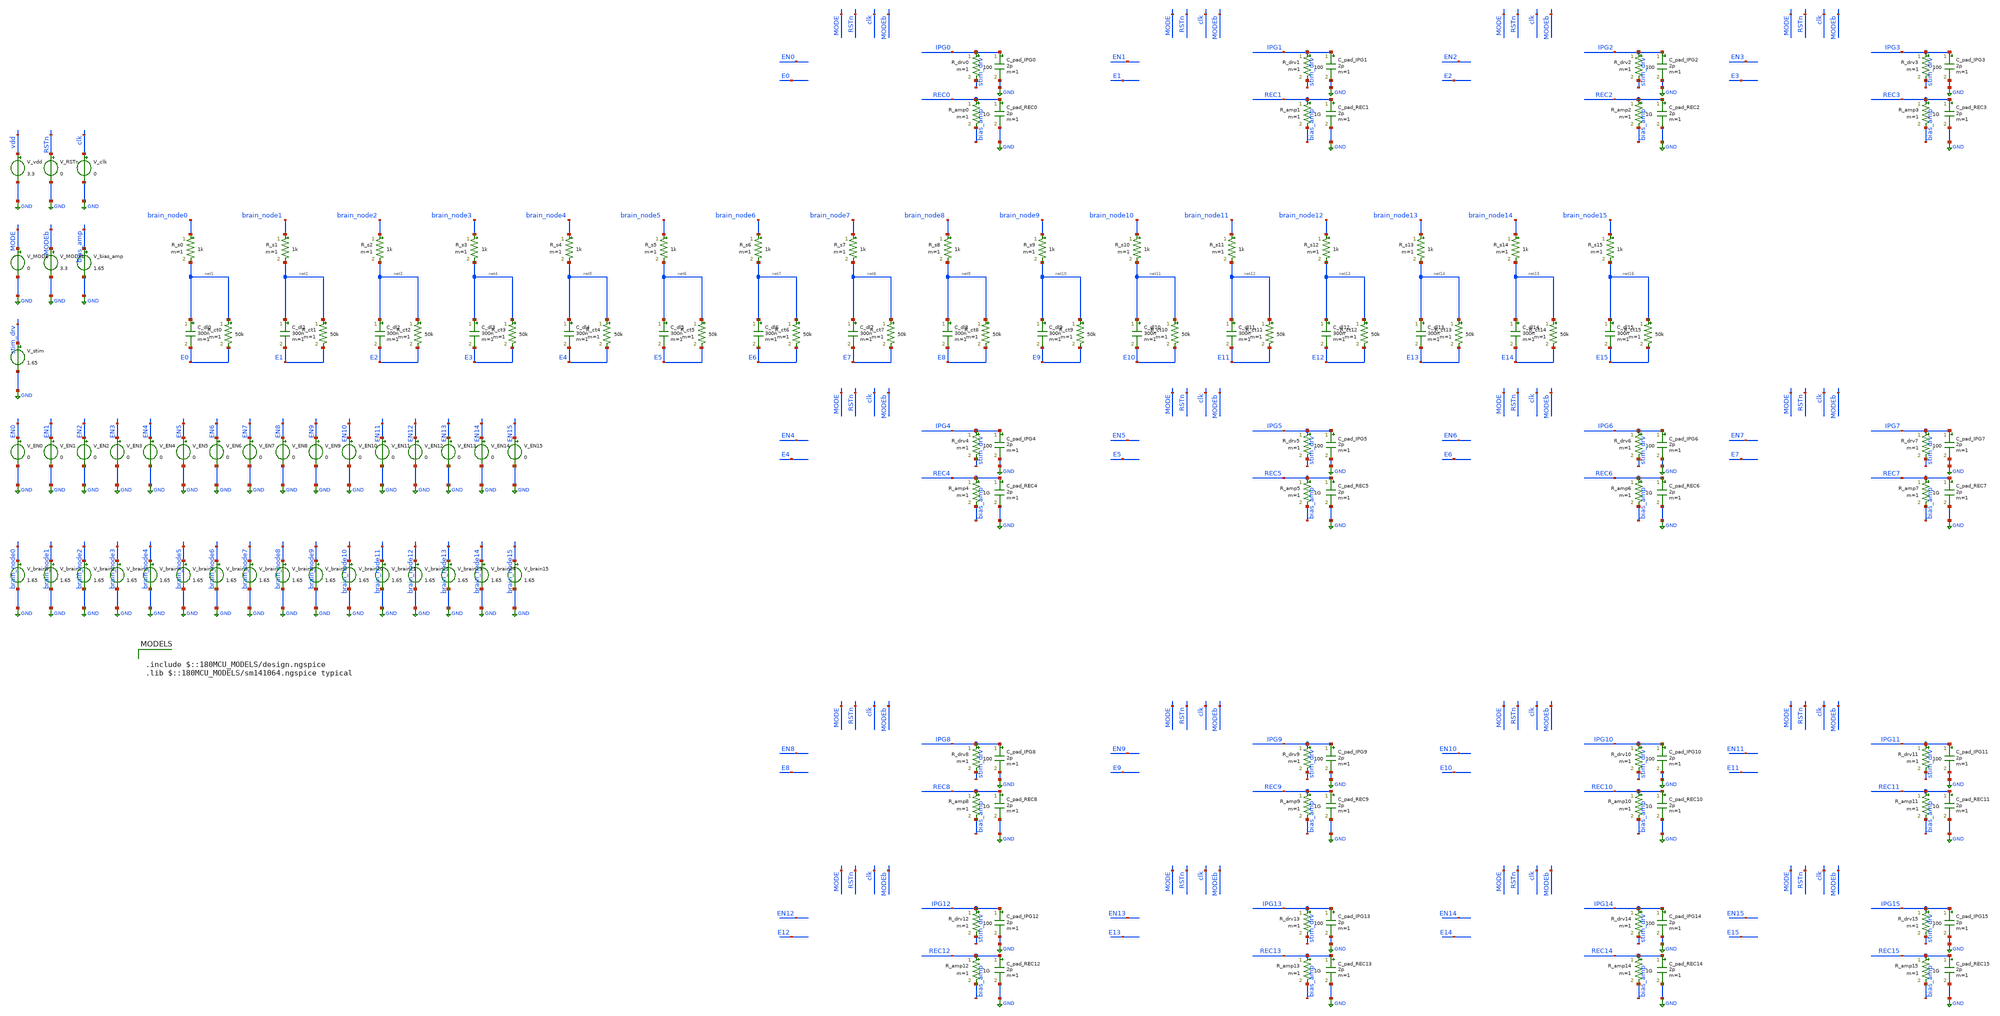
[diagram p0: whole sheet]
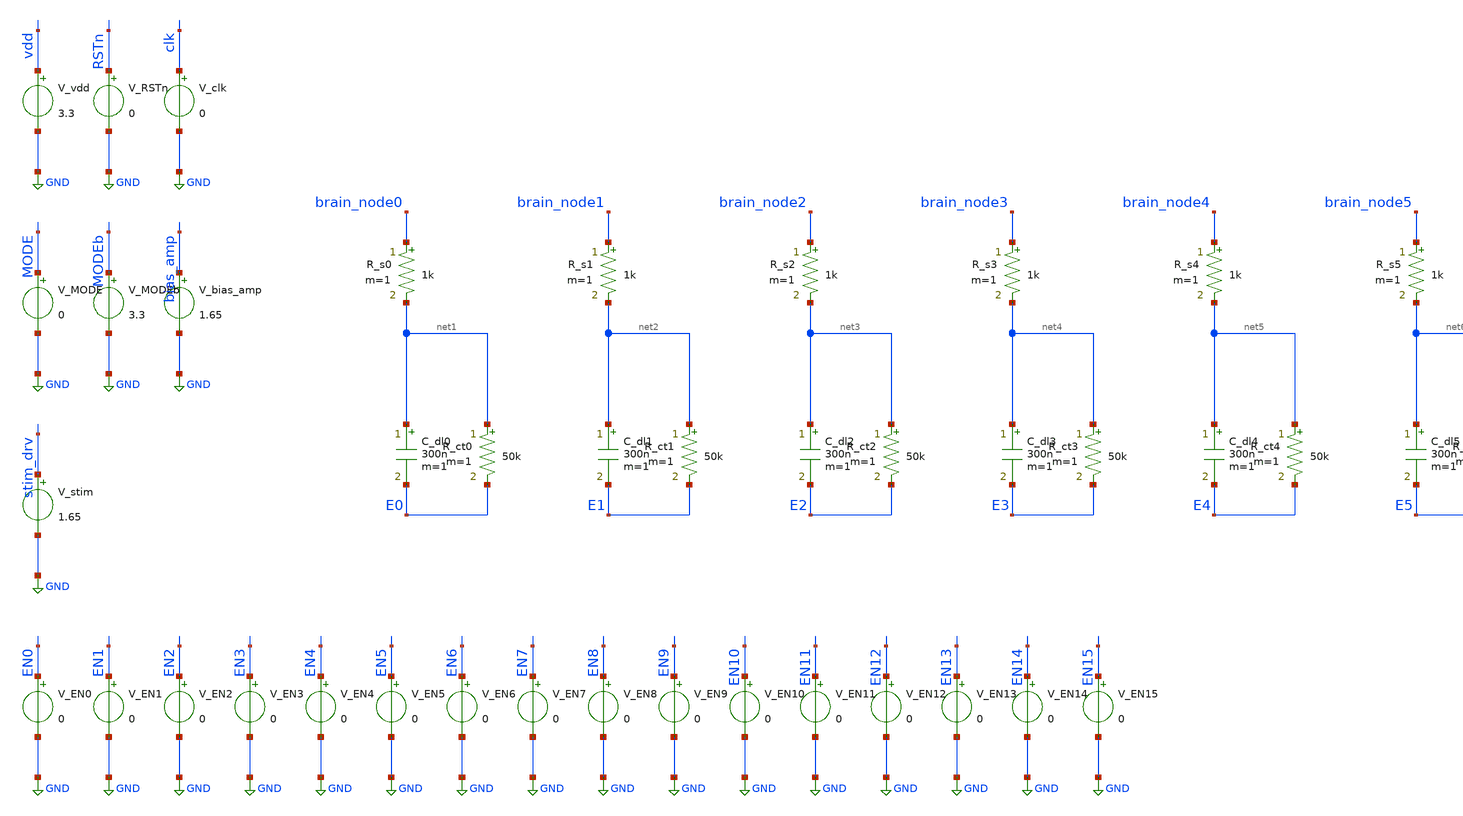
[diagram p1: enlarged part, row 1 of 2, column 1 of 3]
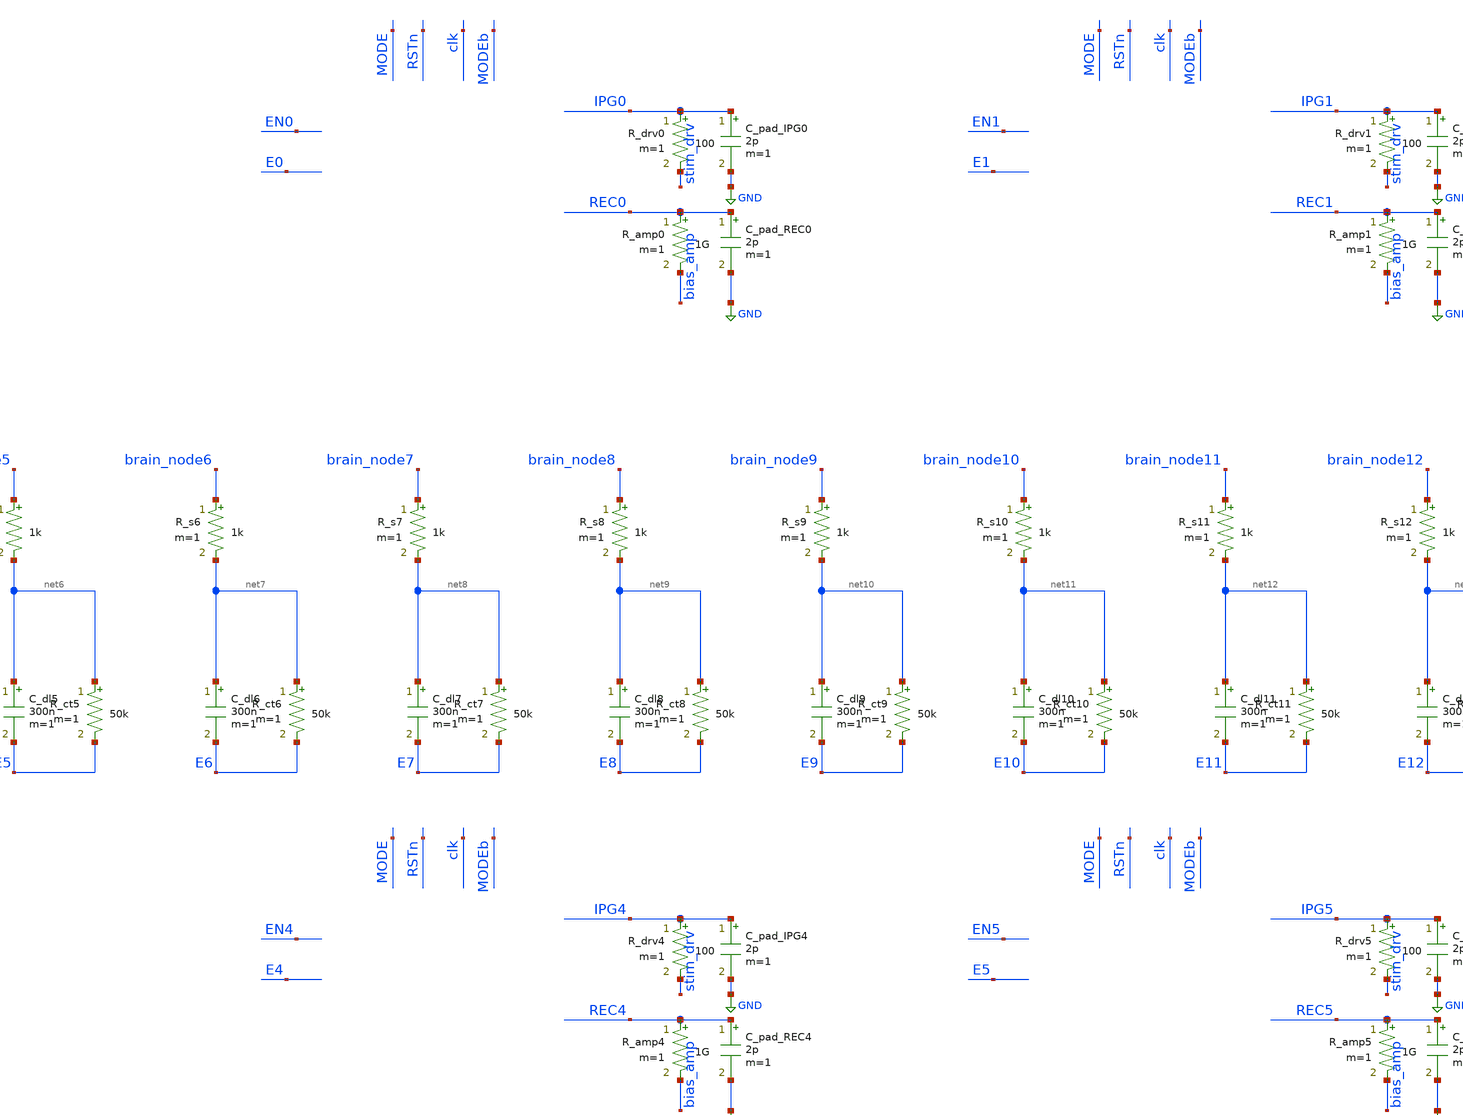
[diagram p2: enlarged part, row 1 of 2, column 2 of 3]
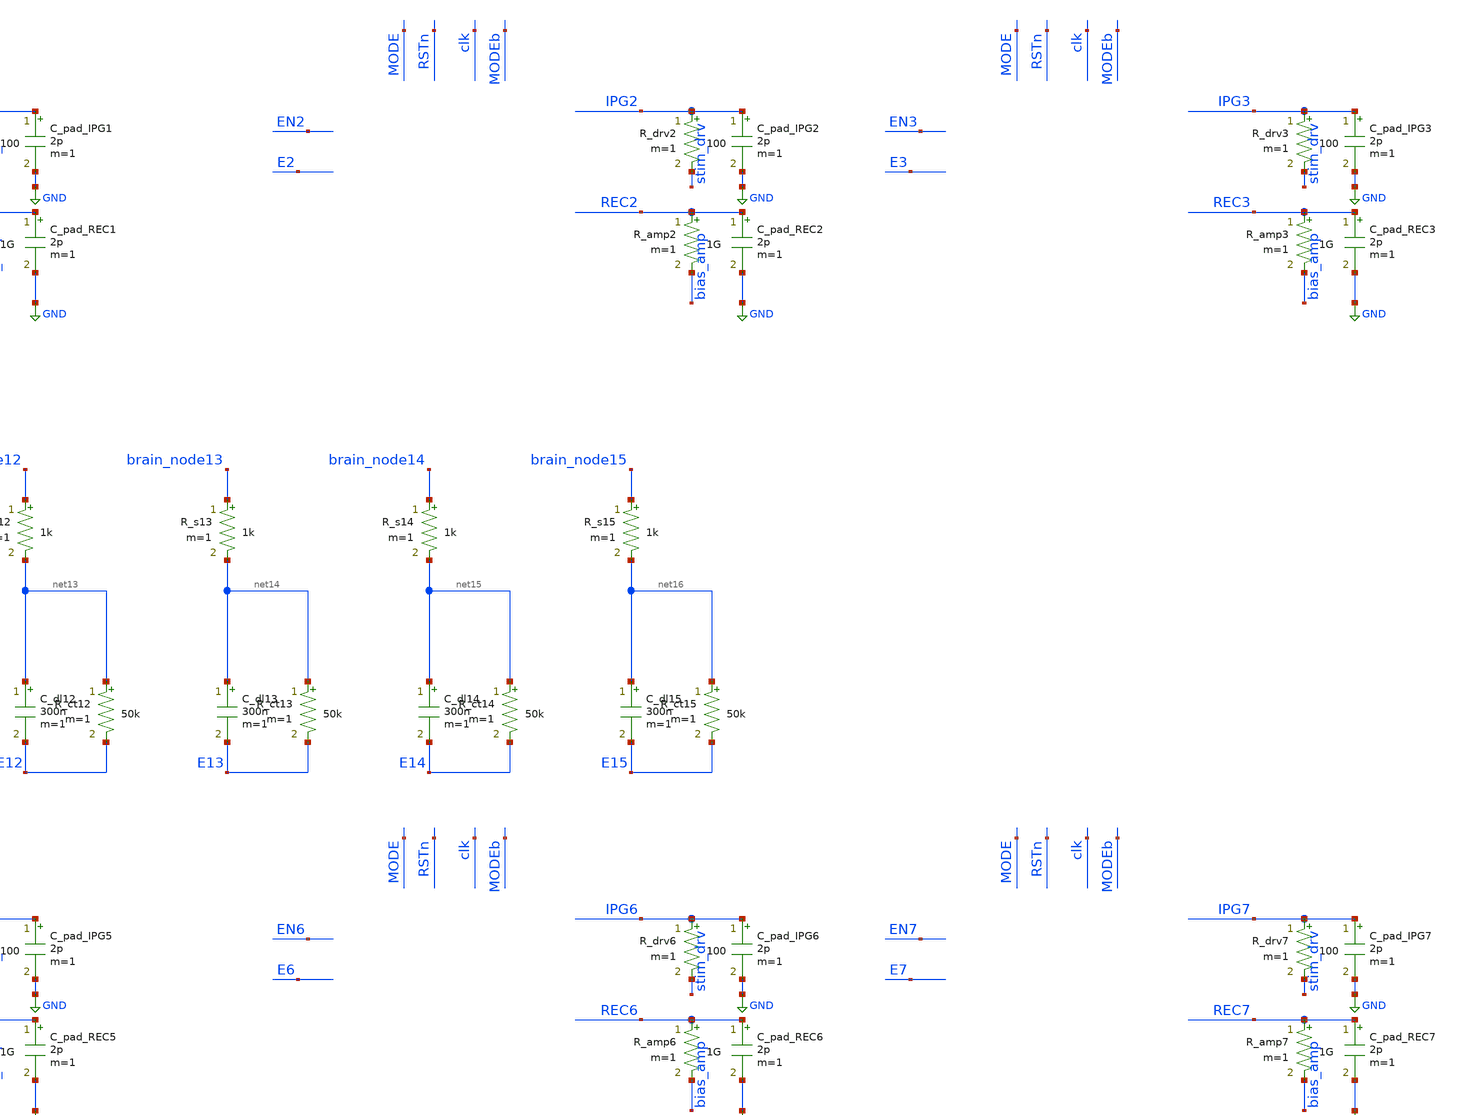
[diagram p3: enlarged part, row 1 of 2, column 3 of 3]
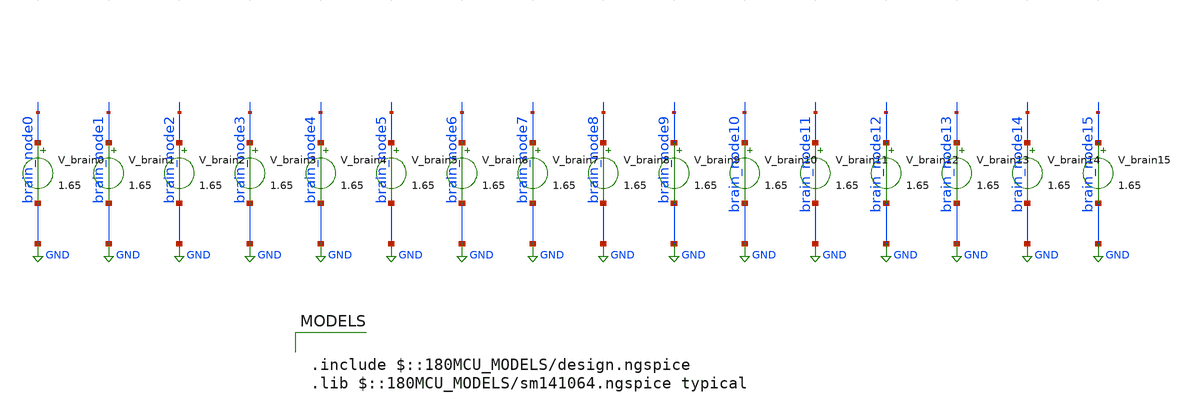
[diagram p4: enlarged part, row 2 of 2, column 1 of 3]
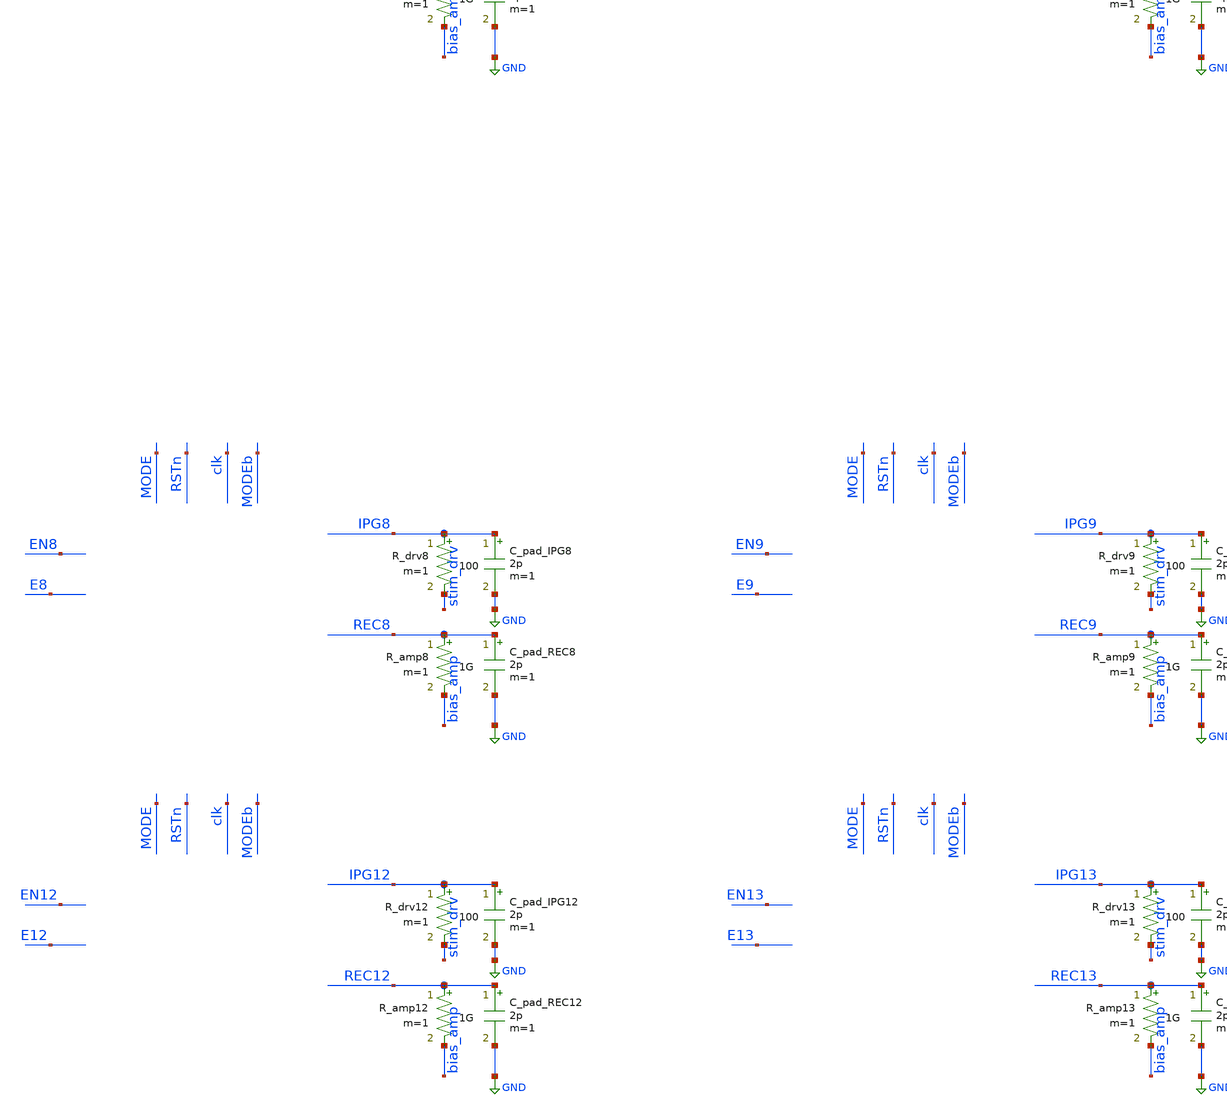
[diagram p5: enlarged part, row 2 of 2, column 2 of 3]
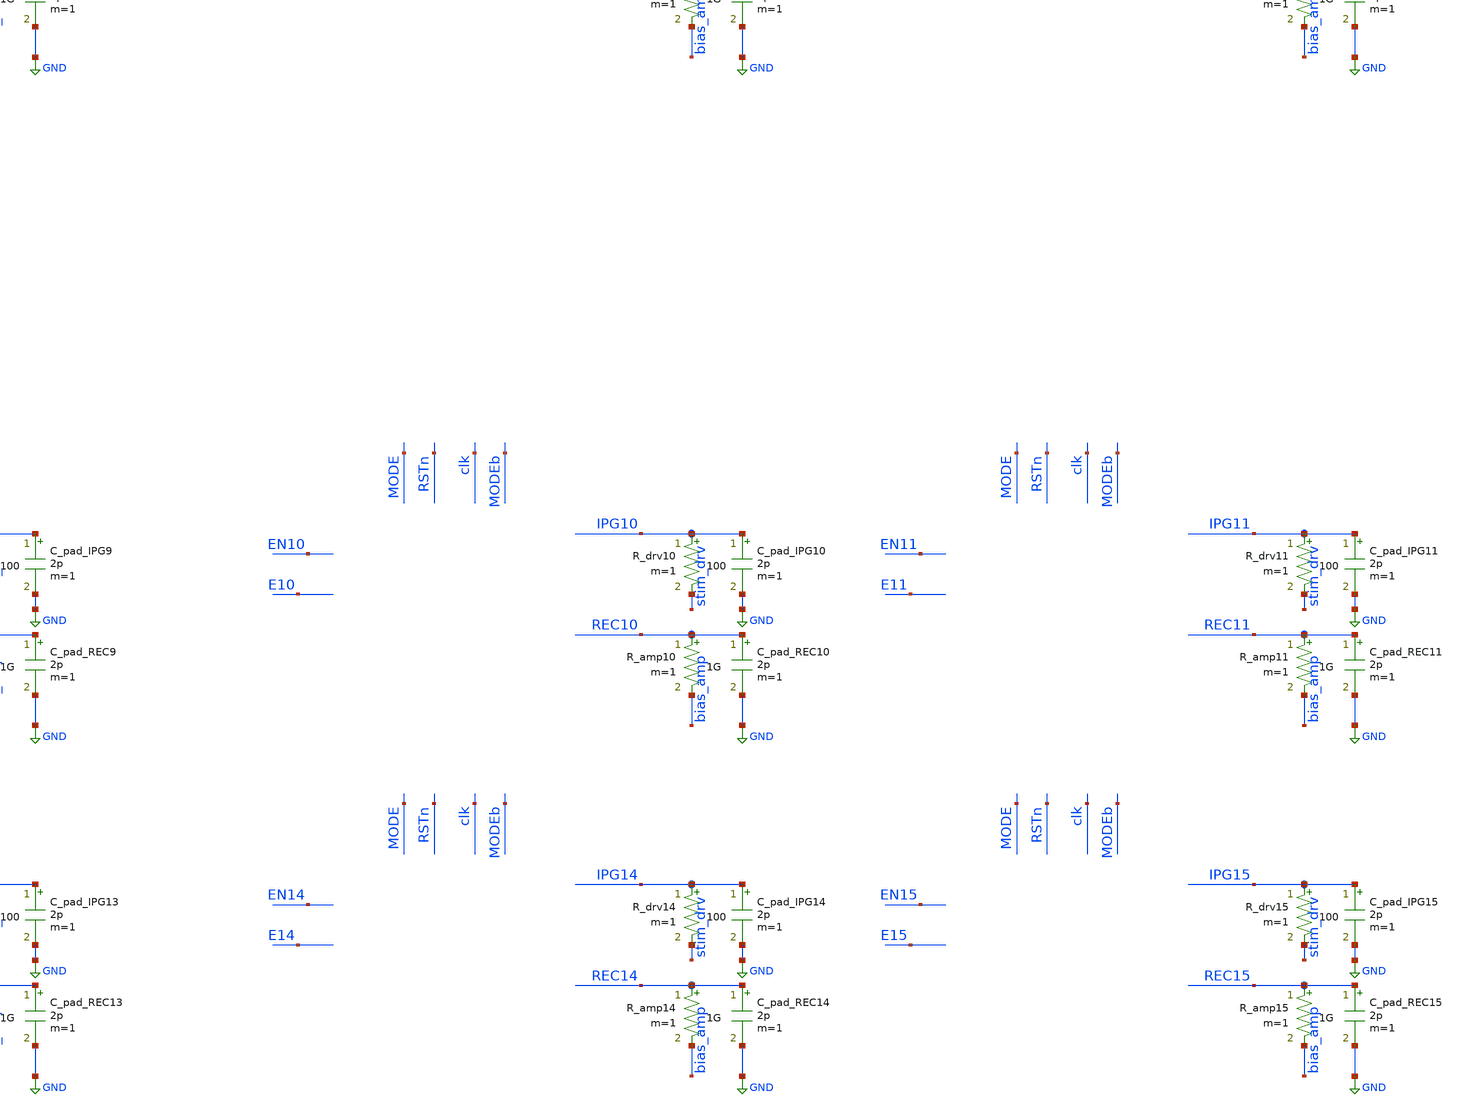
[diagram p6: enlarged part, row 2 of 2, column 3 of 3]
** sch_path: tb_realistic_16ch_postPEX.sch
**.subckt tb_realistic_16ch_postPEX
V_vdd vdd GND 3.3
V_RSTn RSTn GND 0
V_clk clk GND 0
V_MODE MODE GND 0
V_MODEb MODEb GND 3.3
V_bias_amp bias_amp GND 1.65
V_stim stim_drv GND 1.65
V_EN0 EN0 GND 0
V_EN1 EN1 GND 0
V_EN2 EN2 GND 0
V_EN3 EN3 GND 0
V_EN4 EN4 GND 0
V_EN5 EN5 GND 0
V_EN6 EN6 GND 0
V_EN7 EN7 GND 0
V_EN8 EN8 GND 0
V_EN9 EN9 GND 0
V_EN10 EN10 GND 0
V_EN11 EN11 GND 0
V_EN12 EN12 GND 0
V_EN13 EN13 GND 0
V_EN14 EN14 GND 0
V_EN15 EN15 GND 0
V_brain0 brain_node0 GND 1.65
V_brain1 brain_node1 GND 1.65
V_brain2 brain_node2 GND 1.65
V_brain3 brain_node3 GND 1.65
V_brain4 brain_node4 GND 1.65
V_brain5 brain_node5 GND 1.65
V_brain6 brain_node6 GND 1.65
V_brain7 brain_node7 GND 1.65
V_brain8 brain_node8 GND 1.65
V_brain9 brain_node9 GND 1.65
V_brain10 brain_node10 GND 1.65
V_brain11 brain_node11 GND 1.65
V_brain12 brain_node12 GND 1.65
V_brain13 brain_node13 GND 1.65
V_brain14 brain_node14 GND 1.65
V_brain15 brain_node15 GND 1.65
R_s0 brain_node0 net1 1k m=1
C_dl0 net1 E0 300n m=1
R_ct0 net1 E0 50k m=1
R_s1 brain_node1 net2 1k m=1
C_dl1 net2 E1 300n m=1
R_ct1 net2 E1 50k m=1
R_s2 brain_node2 net3 1k m=1
C_dl2 net3 E2 300n m=1
R_ct2 net3 E2 50k m=1
R_s3 brain_node3 net4 1k m=1
C_dl3 net4 E3 300n m=1
R_ct3 net4 E3 50k m=1
R_s4 brain_node4 net5 1k m=1
C_dl4 net5 E4 300n m=1
R_ct4 net5 E4 50k m=1
R_s5 brain_node5 net6 1k m=1
C_dl5 net6 E5 300n m=1
R_ct5 net6 E5 50k m=1
R_s6 brain_node6 net7 1k m=1
C_dl6 net7 E6 300n m=1
R_ct6 net7 E6 50k m=1
R_s7 brain_node7 net8 1k m=1
C_dl7 net8 E7 300n m=1
R_ct7 net8 E7 50k m=1
R_s8 brain_node8 net9 1k m=1
C_dl8 net9 E8 300n m=1
R_ct8 net9 E8 50k m=1
R_s9 brain_node9 net10 1k m=1
C_dl9 net10 E9 300n m=1
R_ct9 net10 E9 50k m=1
R_s10 brain_node10 net11 1k m=1
C_dl10 net11 E10 300n m=1
R_ct10 net11 E10 50k m=1
R_s11 brain_node11 net12 1k m=1
C_dl11 net12 E11 300n m=1
R_ct11 net12 E11 50k m=1
R_s12 brain_node12 net13 1k m=1
C_dl12 net13 E12 300n m=1
R_ct12 net13 E12 50k m=1
R_s13 brain_node13 net14 1k m=1
C_dl13 net14 E13 300n m=1
R_ct13 net14 E13 50k m=1
R_s14 brain_node14 net15 1k m=1
C_dl14 net15 E14 300n m=1
R_ct14 net15 E14 50k m=1
R_s15 brain_node15 net16 1k m=1
C_dl15 net16 E15 300n m=1
R_ct15 net16 E15 50k m=1
R_drv0 IPG0 stim_drv 100 m=1
C_pad_IPG0 IPG0 GND 2p m=1
R_amp0 REC0 bias_amp 1G m=1
C_pad_REC0 REC0 GND 2p m=1
R_drv1 IPG1 stim_drv 100 m=1
C_pad_IPG1 IPG1 GND 2p m=1
R_amp1 REC1 bias_amp 1G m=1
C_pad_REC1 REC1 GND 2p m=1
R_drv2 IPG2 stim_drv 100 m=1
C_pad_IPG2 IPG2 GND 2p m=1
R_amp2 REC2 bias_amp 1G m=1
C_pad_REC2 REC2 GND 2p m=1
R_drv3 IPG3 stim_drv 100 m=1
C_pad_IPG3 IPG3 GND 2p m=1
R_amp3 REC3 bias_amp 1G m=1
C_pad_REC3 REC3 GND 2p m=1
R_drv4 IPG4 stim_drv 100 m=1
C_pad_IPG4 IPG4 GND 2p m=1
R_amp4 REC4 bias_amp 1G m=1
C_pad_REC4 REC4 GND 2p m=1
R_drv5 IPG5 stim_drv 100 m=1
C_pad_IPG5 IPG5 GND 2p m=1
R_amp5 REC5 bias_amp 1G m=1
C_pad_REC5 REC5 GND 2p m=1
R_drv6 IPG6 stim_drv 100 m=1
C_pad_IPG6 IPG6 GND 2p m=1
R_amp6 REC6 bias_amp 1G m=1
C_pad_REC6 REC6 GND 2p m=1
R_drv7 IPG7 stim_drv 100 m=1
C_pad_IPG7 IPG7 GND 2p m=1
R_amp7 REC7 bias_amp 1G m=1
C_pad_REC7 REC7 GND 2p m=1
R_drv8 IPG8 stim_drv 100 m=1
C_pad_IPG8 IPG8 GND 2p m=1
R_amp8 REC8 bias_amp 1G m=1
C_pad_REC8 REC8 GND 2p m=1
R_drv9 IPG9 stim_drv 100 m=1
C_pad_IPG9 IPG9 GND 2p m=1
R_amp9 REC9 bias_amp 1G m=1
C_pad_REC9 REC9 GND 2p m=1
R_drv10 IPG10 stim_drv 100 m=1
C_pad_IPG10 IPG10 GND 2p m=1
R_amp10 REC10 bias_amp 1G m=1
C_pad_REC10 REC10 GND 2p m=1
R_drv11 IPG11 stim_drv 100 m=1
C_pad_IPG11 IPG11 GND 2p m=1
R_amp11 REC11 bias_amp 1G m=1
C_pad_REC11 REC11 GND 2p m=1
R_drv12 IPG12 stim_drv 100 m=1
C_pad_IPG12 IPG12 GND 2p m=1
R_amp12 REC12 bias_amp 1G m=1
C_pad_REC12 REC12 GND 2p m=1
R_drv13 IPG13 stim_drv 100 m=1
C_pad_IPG13 IPG13 GND 2p m=1
R_amp13 REC13 bias_amp 1G m=1
C_pad_REC13 REC13 GND 2p m=1
R_drv14 IPG14 stim_drv 100 m=1
C_pad_IPG14 IPG14 GND 2p m=1
R_amp14 REC14 bias_amp 1G m=1
C_pad_REC14 REC14 GND 2p m=1
R_drv15 IPG15 stim_drv 100 m=1
C_pad_IPG15 IPG15 GND 2p m=1
R_amp15 REC15 bias_amp 1G m=1
C_pad_REC15 REC15 GND 2p m=1
**** begin user architecture code

.include $::180MCU_MODELS/design.ngspice
.lib $::180MCU_MODELS/sm141064.ngspice typical



.control
save all

** RSTn: low until 100ns then high
alter @V_RSTn[PWL] = [ 0 0  100n 0  100.001n 3.3  30m 3.3 ]

** Single latching clock pulse around 200ns
alter @V_clk[PWL] = [ 0 0  200n 0  200.001n 3.3  300n 3.3  300.001n 0  30m 0 ]

** EN[0..15]: all high after RSTn release
alter @V_EN0[PWL] = [ 0 0  150n 0  150.001n 3.3  30m 3.3 ]
alter @V_EN1[PWL] = [ 0 0  150n 0  150.001n 3.3  30m 3.3 ]
alter @V_EN2[PWL] = [ 0 0  150n 0  150.001n 3.3  30m 3.3 ]
alter @V_EN3[PWL] = [ 0 0  150n 0  150.001n 3.3  30m 3.3 ]
alter @V_EN4[PWL] = [ 0 0  150n 0  150.001n 3.3  30m 3.3 ]
alter @V_EN5[PWL] = [ 0 0  150n 0  150.001n 3.3  30m 3.3 ]
alter @V_EN6[PWL] = [ 0 0  150n 0  150.001n 3.3  30m 3.3 ]
alter @V_EN7[PWL] = [ 0 0  150n 0  150.001n 3.3  30m 3.3 ]
alter @V_EN8[PWL] = [ 0 0  150n 0  150.001n 3.3  30m 3.3 ]
alter @V_EN9[PWL] = [ 0 0  150n 0  150.001n 3.3  30m 3.3 ]
alter @V_EN10[PWL] = [ 0 0  150n 0  150.001n 3.3  30m 3.3 ]
alter @V_EN11[PWL] = [ 0 0  150n 0  150.001n 3.3  30m 3.3 ]
alter @V_EN12[PWL] = [ 0 0  150n 0  150.001n 3.3  30m 3.3 ]
alter @V_EN13[PWL] = [ 0 0  150n 0  150.001n 3.3  30m 3.3 ]
alter @V_EN14[PWL] = [ 0 0  150n 0  150.001n 3.3  30m 3.3 ]
alter @V_EN15[PWL] = [ 0 0  150n 0  150.001n 3.3  30m 3.3 ]

** MODE: stim phase 0-15ms (includes drain), record phase 15-30ms
alter @V_MODE[PWL]  = [ 0 0    15m 0    15.0001m 3.3   30m 3.3 ]
alter @V_MODEb[PWL] = [ 0 3.3  15m 3.3  15.0001m 0     30m 0 ]

** Brain LFPs: 100uV (10mV in source units, see scaling) 1kHz sines on 1.65V mid-rail,
** with 22.5deg phase increments per channel so REC traces are visually distinguishable.
alter @V_brain0[SIN] = [ 1.65 10m 1k 0 0 0.0000 ]
alter @V_brain1[SIN] = [ 1.65 10m 1k 0 0 22.5000 ]
alter @V_brain2[SIN] = [ 1.65 10m 1k 0 0 45.0000 ]
alter @V_brain3[SIN] = [ 1.65 10m 1k 0 0 67.5000 ]
alter @V_brain4[SIN] = [ 1.65 10m 1k 0 0 90.0000 ]
alter @V_brain5[SIN] = [ 1.65 10m 1k 0 0 112.5000 ]
alter @V_brain6[SIN] = [ 1.65 10m 1k 0 0 135.0000 ]
alter @V_brain7[SIN] = [ 1.65 10m 1k 0 0 157.5000 ]
alter @V_brain8[SIN] = [ 1.65 10m 1k 0 0 180.0000 ]
alter @V_brain9[SIN] = [ 1.65 10m 1k 0 0 202.5000 ]
alter @V_brain10[SIN] = [ 1.65 10m 1k 0 0 225.0000 ]
alter @V_brain11[SIN] = [ 1.65 10m 1k 0 0 247.5000 ]
alter @V_brain12[SIN] = [ 1.65 10m 1k 0 0 270.0000 ]
alter @V_brain13[SIN] = [ 1.65 10m 1k 0 0 292.5000 ]
alter @V_brain14[SIN] = [ 1.65 10m 1k 0 0 315.0000 ]
alter @V_brain15[SIN] = [ 1.65 10m 1k 0 0 337.5000 ]

** Stim driver: biphasic pulses at 0.5/1.5/2.5/3.5/4.5 ms during stim phase,
** then held at mid-rail for 10 ms drain before MODE switches.
alter @V_stim[PWL] = [  0          1.65  500u       1.65  500.001u   0.65  600u       0.65  600.001u
+   2.65  700u       2.65  700.001u   1.65  1500u      1.65  1500.001u  0.65  1600u      0.65  1600.001u
+  2.65  1700u      2.65  1700.001u  1.65  2500u      1.65  2500.001u  0.65  2600u      0.65  2600.001u
+  2.65  2700u      2.65  2700.001u  1.65  3500u      1.65  3500.001u  0.65  3600u      0.65  3600.001u
+  2.65  3700u      2.65  3700.001u  1.65  4500u      1.65  4500.001u  0.65  4600u      0.65  4600.001u
+  2.65  4700u      2.65  4700.001u  1.65  30m        1.65 ]

tran 1u 30m 0 5u

** plots
set color0 = white
set nolegend

** Plot a representative 4 channels (0,4,8,12): MODE marker, REC traces, E traces, scaled IPG traces
plot (v(MODE)*16.65/3.3)+0.825 v(REC0) v(REC1)+1 v(REC2)+2 v(REC3)+3 v(REC4)+4 v(REC5)+5 v(REC6)+6
+ v(REC7)+7 v(REC8)+8 v(REC9)+9 v(REC10)+10 v(REC11)+11 v(REC12)+12 v(REC13)+13 v(REC14)+14 v(REC15)+15 v(E0)
+ v(E1)+1 v(E2)+2 v(E3)+3 v(E4)+4 v(E5)+5 v(E6)+6 v(E7)+7 v(E8)+8 v(E9)+9 v(E10)+10 v(E11)+11 v(E12)+12
+ v(E13)+13 v(E14)+14 v(E15)+15 v(IPG0)/3+(1.65-1.65/3) (v(IPG1)/3+(1.65-1.65/3))+1 (v(IPG2)/3+(1.65-1.65/3))+2
+ (v(IPG3)/3+(1.65-1.65/3))+3 (v(IPG4)/3+(1.65-1.65/3))+4 (v(IPG5)/3+(1.65-1.65/3))+5 (v(IPG6)/3+(1.65-1.65/3))+6
+ (v(IPG7)/3+(1.65-1.65/3))+7 (v(IPG8)/3+(1.65-1.65/3))+8 (v(IPG9)/3+(1.65-1.65/3))+9 (v(IPG10)/3+(1.65-1.65/3))+10
+ (v(IPG11)/3+(1.65-1.65/3))+11 (v(IPG12)/3+(1.65-1.65/3))+12 (v(IPG13)/3+(1.65-1.65/3))+13 (v(IPG14)/3+(1.65-1.65/3))+14
+ (v(IPG15)/3+(1.65-1.65/3))+15
plot v(REC0) v(REC1)+0.1 v(REC2)+0.2 v(REC3)+0.3 v(REC4)+0.4 v(REC5)+0.5 v(REC6)+0.6 v(REC7)+0.7
+ v(REC8)+0.8 v(REC9)+0.9 v(REC10)+1 v(REC11)+1.1 v(REC12)+1.2 v(REC13)+1.3 v(REC14)+1.4 v(REC15)+1.5 v(E0)
+ v(E1)+0.1 v(E2)+0.2 v(E3)+0.3 v(E4)+0.4 v(E5)+0.5 v(E6)+0.6 v(E7)+0.7 v(E8)+0.8 v(E9)+0.9 v(E10)+1 v(E11)+1.1
+ v(E12)+1.2 v(E13)+1.3 v(E14)+1.4 v(E15)+1.5 v(IPG0)/3+(1.65-1.65/3) (v(IPG1)/3+(1.65-1.65/3))+0.1
+ (v(IPG2)/3+(1.65-1.65/3))+0.2 (v(IPG3)/3+(1.65-1.65/3))+0.3 (v(IPG4)/3+(1.65-1.65/3))+0.4 (v(IPG5)/3+(1.65-1.65/3))+0.5
+ (v(IPG6)/3+(1.65-1.65/3))+0.6 (v(IPG7)/3+(1.65-1.65/3))+0.7 (v(IPG8)/3+(1.65-1.65/3))+0.8 (v(IPG9)/3+(1.65-1.65/3))+0.9
+ (v(IPG10)/3+(1.65-1.65/3))+1 (v(IPG11)/3+(1.65-1.65/3))+1.1 (v(IPG12)/3+(1.65-1.65/3))+1.2 (v(IPG13)/3+(1.65-1.65/3))+1.3
+ (v(IPG14)/3+(1.65-1.65/3))+1.4 (v(IPG15)/3+(1.65-1.65/3))+1.5 xlimit 14m 30m ylimit 1.6 3.2
plot v(REC0) v(REC1)+1 v(REC2)+2 v(REC3)+3 v(REC4)+4 v(REC5)+5 v(REC6)+6 v(REC7)+7 v(REC8)+8
+ v(REC9)+9 v(REC10)+10 v(REC11)+11 v(REC12)+12 v(REC13)+13 v(REC14)+14 v(REC15)+15 v(E0) v(E1)+1 v(E2)+2
+ v(E3)+3 v(E4)+4 v(E5)+5 v(E6)+6 v(E7)+7 v(E8)+8 v(E9)+9 v(E10)+10 v(E11)+11 v(E12)+12 v(E13)+13 v(E14)+14
+ v(E15)+15 v(IPG0)/3+(1.65-1.65/3) (v(IPG1)/3+(1.65-1.65/3))+1 (v(IPG2)/3+(1.65-1.65/3))+2
+ (v(IPG3)/3+(1.65-1.65/3))+3 (v(IPG4)/3+(1.65-1.65/3))+4 (v(IPG5)/3+(1.65-1.65/3))+5 (v(IPG6)/3+(1.65-1.65/3))+6
+ (v(IPG7)/3+(1.65-1.65/3))+7 (v(IPG8)/3+(1.65-1.65/3))+8 (v(IPG9)/3+(1.65-1.65/3))+9 (v(IPG10)/3+(1.65-1.65/3))+10
+ (v(IPG11)/3+(1.65-1.65/3))+11 (v(IPG12)/3+(1.65-1.65/3))+12 (v(IPG13)/3+(1.65-1.65/3))+13 (v(IPG14)/3+(1.65-1.65/3))+14
+ (v(IPG15)/3+(1.65-1.65/3))+15 xlimit 0m 5m
write tb_realistic_16ch.raw
.endc




.SUBCKT ROW VDD E REC RSTn EN CLK MODE GND IPG MODEb
M1 n8 n7 VDD VDD pfet_03v3 L=0.28U W=1U AS=0.65P AD=0.42P PS=3.3U PD=1.84U
M2 VDD n20 n8 VDD pfet_03v3 L=0.28U W=1U AS=0.42P AD=0.735P PS=1.84U PD=2.47U
M3 n9 n8 VDD VDD pfet_03v3 L=0.28U W=1U AS=0.735P AD=0.635P PS=2.47U PD=3.27U
M4 n10 n9 VDD VDD pfet_03v3 L=0.28U W=1U AS=0.55P AD=0.65P PS=3.1U PD=3.3U
M5 REC n10 E VDD pfet_03v3 L=0.28U W=1U AS=0.65P AD=0.65P PS=3.3U PD=3.3U
M6 n3 n13 VDD VDD pfet_03v3 L=0.28U W=1U AS=0.76P AD=0.65P PS=3.52U PD=3.3U
M7 VDD n3 n4 VDD pfet_03v3 L=0.28U W=1U AS=0.65P AD=0.65P PS=3.3U PD=3.3U
M8 n4 RSTn VDD VDD pfet_03v3 L=0.28U W=1U AS=0.65P AD=0.65P PS=3.3U PD=3.3U
M9 n13 n2 n4 VDD pfet_03v3 L=0.28U W=1U AS=0.65P AD=0.59P PS=3.3U PD=3.18U
M10 n5 EN n13 VDD pfet_03v3 L=0.28U W=1U AS=0.63P AD=0.605P PS=3.26U PD=3.21U
M11 VDD n15 n5 VDD pfet_03v3 L=0.28U W=1U AS=0.63P AD=0.54P PS=3.26U PD=3.08U
M12 VDD n2 n15 VDD pfet_03v3 L=0.28U W=1U AS=0.63P AD=0.64P PS=3.26U PD=3.28U
M13 VDD CLK n2 VDD pfet_03v3 L=0.28U W=1U AS=0.65P AD=0.65P PS=3.3U PD=3.3U
M14 n6 MODE VDD VDD pfet_03v3 L=0.28U W=1U AS=0.65P AD=0.42P PS=3.3U PD=1.84U
M15 VDD n18 n6 VDD pfet_03v3 L=0.28U W=1U AS=0.42P AD=0.735P PS=1.84U  PD=2.47U
M16 n7 n6 VDD VDD pfet_03v3 L=0.28U W=1U AS=0.735P AD=0.64P PS=2.47U PD=3.28U
M17 n56 n54 VDD VDD pfet_03v3 L=0.28U W=1U AS=0.65P AD=0.65P PS=3.3U PD=3.3U
M18 n85 n56 n54 VDD pfet_03v3 L=0.28U W=1U AS=0.65P AD=0.65P PS=3.3U PD=3.3U
M19 VDD n15 n85 VDD pfet_03v3 L=0.28U W=1U AS=0.65P AD=0.65P PS=3.3U PD=3.3U
M20 n18 n56 VDD VDD pfet_03v3 L=0.28U W=1U AS=0.65P AD=0.65P PS=3.3U PD=3.3U
M21 n58 n56 VDD VDD pfet_03v3 L=0.28U W=1U AS=0.65P AD=0.65P PS=3.3U PD=3.3U
M22 n59 n58 VDD VDD pfet_03v3 L=0.28U W=1U AS=0.65P AD=0.65P PS=3.3U PD=3.3U
M23 n60 MODEb VDD VDD pfet_03v3 L=0.28U W=1U AS=0.65P AD=0.42P PS=3.3U  PD=1.84U
M24 VDD n18 n60 VDD pfet_03v3 L=0.28U W=1U AS=0.42P AD=0.735P PS=1.84U  PD=2.47U
M25 n67 n60 VDD VDD pfet_03v3 L=0.28U W=1U AS=0.735P AD=0.63P PS=2.47U  PD=3.26U
M26 n54 n2 n3 VDD pfet_03v3 L=0.28U W=1U AS=0.65P AD=0.65P PS=3.3U PD=3.3U
M27 n56 RSTn VDD VDD pfet_03v3 L=0.28U W=1U AS=0.65P AD=0.65P PS=3.3U PD=3.3U
M28 n61 n67 VDD VDD pfet_03v3 L=0.28U W=1U AS=0.65P AD=0.42P PS=3.3U PD=1.84U
M29 VDD n10 n61 VDD pfet_03v3 L=0.28U W=1U AS=0.42P AD=0.735P PS=1.84U  PD=2.47U
M30 n68 n61 VDD VDD pfet_03v3 L=0.28U W=1U AS=0.735P AD=0.63P PS=2.47U  PD=3.26U
M31 n20 n68 VDD VDD pfet_03v3 L=0.28U W=1U AS=0.56P AD=0.65P PS=3.12U PD=3.3U
M32 IPG n20 E VDD pfet_03v3 L=0.28U W=1U AS=0.65P AD=0.65P PS=3.3U PD=3.3U
M33 n9 n8 GND GND nfet_03v3 L=0.28U W=0.5U AS=0.2425P AD=0.315P PS=1.97U  PD=2.26U
M34 n10 n9 GND GND nfet_03v3 L=0.28U W=0.5U AS=0.2825P AD=0.315P PS=2.13U  PD=2.26U
M35 n7 n6 GND GND nfet_03v3 L=0.28U W=0.5U AS=0.2425P AD=0.3125P PS=1.97U  PD=2.25U
M36 n52 n7 GND GND nfet_03v3 L=0.28U W=1U AS=0.63P AD=0.42P PS=3.26U PD=1.84U
M37 n8 n20 n52 GND nfet_03v3 L=0.28U W=1U AS=0.42P AD=0.65P PS=1.84U PD=3.3U
M38 REC n9 E GND nfet_03v3 L=0.28U W=1U AS=0.63P AD=0.63P PS=3.26U PD=3.26U
M39 n3 n13 GND GND nfet_03v3 L=0.28U W=1U AS=0.76P AD=0.61P PS=3.52U PD=3.22U
M40 n34 n3 GND GND nfet_03v3 L=0.28U W=1U AS=0.61P AD=0.61P PS=3.22U PD=3.22U
M41 n4 RSTn n34 GND nfet_03v3 L=0.28U W=1U AS=0.61P AD=0.61P PS=3.22U  PD=3.22U
M42 n13 n15 n4 GND nfet_03v3 L=0.28U W=1U AS=0.61P AD=0.61P PS=3.22U  PD=3.22U
M43 n35 EN n13 GND nfet_03v3 L=0.28U W=1U AS=0.61P AD=0.61P PS=3.22U PD=3.22U
M44 GND n2 n35 GND nfet_03v3 L=0.28U W=1U AS=0.61P AD=0.575P PS=3.22U  PD=3.15U
M45 GND n2 n15 GND nfet_03v3 L=0.28U W=1U AS=0.61P AD=0.61P PS=3.22U PD=3.22U
M46 GND CLK n2 GND nfet_03v3 L=0.28U W=1U AS=0.63P AD=0.67P PS=3.26U PD=3.34U
M47 n47 MODE GND GND nfet_03v3 L=0.28U W=1U AS=0.63P AD=0.42P PS=3.26U  PD=1.84U
M48 n6 n18 n47 GND nfet_03v3 L=0.28U W=1U AS=0.42P AD=0.65P PS=1.84U PD=3.3U
M49 n54 n15 n3 GND nfet_03v3 L=0.28U W=1U AS=0.715P AD=0.61P PS=3.43U  PD=3.22U
M50 n55 RSTn GND GND nfet_03v3 L=0.28U W=1U AS=0.61P AD=0.61P PS=3.22U  PD=3.22U
M51 n56 n54 n55 GND nfet_03v3 L=0.28U W=1U AS=0.61P AD=0.61P PS=3.22U  PD=3.22U
M52 n57 n56 n54 GND nfet_03v3 L=0.28U W=1U AS=0.61P AD=0.61P PS=3.22U  PD=3.22U
M53 GND n2 n57 GND nfet_03v3 L=0.28U W=1U AS=0.61P AD=0.61P PS=3.22U PD=3.22U
M54 n18 n56 GND GND nfet_03v3 L=0.28U W=1U AS=0.61P AD=0.61P PS=3.22U  PD=3.22U
M55 n58 n56 GND GND nfet_03v3 L=0.28U W=1U AS=0.61P AD=0.61P PS=3.22U  PD=3.22U
M56 n59 n58 GND GND nfet_03v3 L=0.28U W=1U AS=0.61P AD=0.61P PS=3.22U  PD=3.22U
M57 n81 MODEb GND GND nfet_03v3 L=0.28U W=1U AS=0.63P AD=0.42P PS=3.26U  PD=1.84U
M58 n60 n18 n81 GND nfet_03v3 L=0.28U W=1U AS=0.42P AD=0.65P PS=1.84U  PD=3.3U
M59 n67 n60 GND GND nfet_03v3 L=0.28U W=0.5U AS=0.2425P AD=0.31P PS=1.97U  PD=2.24U
M60 n82 n67 GND GND nfet_03v3 L=0.28U W=1U AS=0.63P AD=0.42P PS=3.26U  PD=1.84U
M61 n61 n10 n82 GND nfet_03v3 L=0.28U W=1U AS=0.42P AD=0.65P PS=1.84U  PD=3.3U
M62 n68 n61 GND GND nfet_03v3 L=0.28U W=0.5U AS=0.2425P AD=0.3275P PS=1.97U  PD=2.31U
M63 n20 n68 GND GND nfet_03v3 L=0.28U W=0.5U AS=0.285P AD=0.315P PS=2.14U  PD=2.26U
M64 IPG n68 E GND nfet_03v3 L=0.28U W=1U AS=0.63P AD=0.63P PS=3.26U PD=3.26U
.ENDS ROW

X0 vdd E0 REC0 RSTn EN0 clk MODE GND IPG0 MODEb ROW
X1 vdd E1 REC1 RSTn EN1 clk MODE GND IPG1 MODEb ROW
X2 vdd E2 REC2 RSTn EN2 clk MODE GND IPG2 MODEb ROW
X3 vdd E3 REC3 RSTn EN3 clk MODE GND IPG3 MODEb ROW
X4 vdd E4 REC4 RSTn EN4 clk MODE GND IPG4 MODEb ROW
X5 vdd E5 REC5 RSTn EN5 clk MODE GND IPG5 MODEb ROW
X6 vdd E6 REC6 RSTn EN6 clk MODE GND IPG6 MODEb ROW
X7 vdd E7 REC7 RSTn EN7 clk MODE GND IPG7 MODEb ROW
X8 vdd E8 REC8 RSTn EN8 clk MODE GND IPG8 MODEb ROW
X9 vdd E9 REC9 RSTn EN9 clk MODE GND IPG9 MODEb ROW
X10 vdd E10 REC10 RSTn EN10 clk MODE GND IPG10 MODEb ROW
X11 vdd E11 REC11 RSTn EN11 clk MODE GND IPG11 MODEb ROW
X12 vdd E12 REC12 RSTn EN12 clk MODE GND IPG12 MODEb ROW
X13 vdd E13 REC13 RSTn EN13 clk MODE GND IPG13 MODEb ROW
X14 vdd E14 REC14 RSTn EN14 clk MODE GND IPG14 MODEb ROW
X15 vdd E15 REC15 RSTn EN15 clk MODE GND IPG15 MODEb ROW


**** end user architecture code
**.ends
.GLOBAL GND
.end
